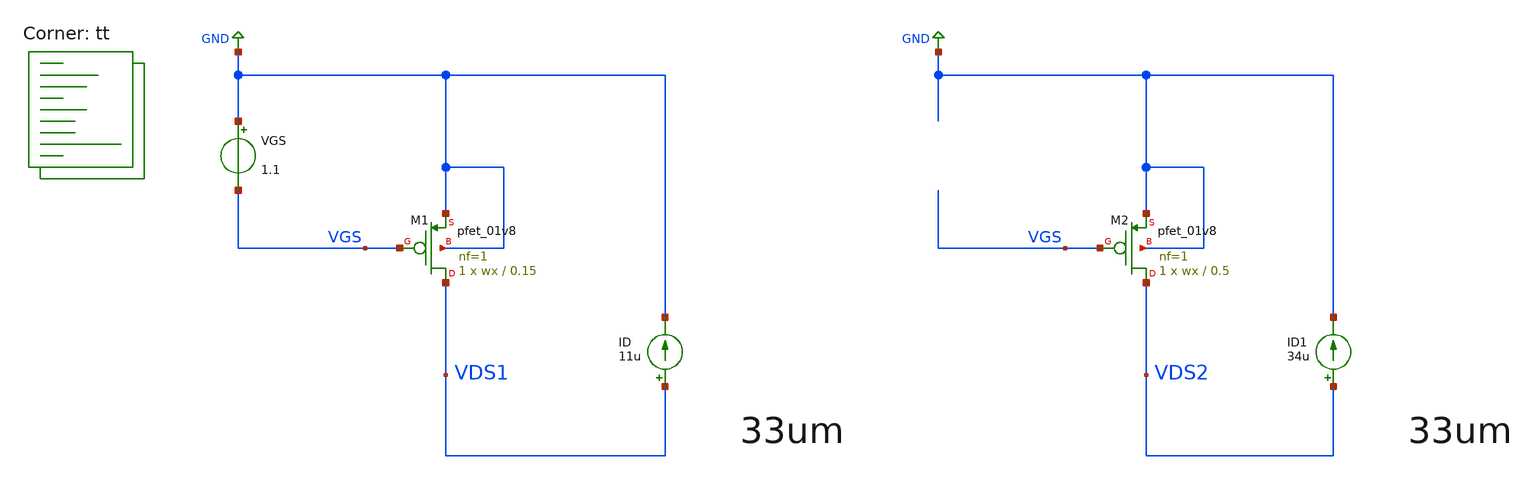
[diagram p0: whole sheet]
** sch_path: projects/opamp/xschem_ngspice/vgs_id_sweep_pfet_2.sch
**.subckt vgs_id_sweep_pfet_2
VGS GND VGS 1.1
ID VDS1 GND 11u
XM1 VDS1 VGS GND GND sky130_fd_pr__pfet_01v8 L=0.15 W=wx nf=1 ad='int((nf+1)/2) * W/nf * 0.29' as='int((nf+2)/2) * W/nf * 0.29'
+ pd='2*int((nf+1)/2) * (W/nf + 0.29)' ps='2*int((nf+2)/2) * (W/nf + 0.29)' nrd='0.29 / W' nrs='0.29 / W'
+ sa=0 sb=0 sd=0 mult=1 m=1
ID1 VDS2 GND 34u
XM2 VDS2 VGS GND GND sky130_fd_pr__pfet_01v8 L=0.5 W=wx nf=1 ad='int((nf+1)/2) * W/nf * 0.29' as='int((nf+2)/2) * W/nf * 0.29'
+ pd='2*int((nf+1)/2) * (W/nf + 0.29)' ps='2*int((nf+2)/2) * (W/nf + 0.29)' nrd='0.29 / W' nrs='0.29 / W'
+ sa=0 sb=0 sd=0 mult=1 m=1
**** begin user architecture code
.lib $::SKYWATER_MODELS/sky130.lib.spice tt




.option method=gear
.option wnflag=1
.option savecurrents

.save @m.xm1.msky130_fd_pr__pfet_01v8[gm] @m.xm1.msky130_fd_pr__pfet_01v8[W] @m.xm1.msky130_fd_pr__pfet_01v8[vth] @m.xm1.msky130_fd_pr__pfet_01v8[gds] @m.xm2.msky130_fd_pr__pfet_01v8[gm] @m.xm2.msky130_fd_pr__pfet_01v8[W] @m.xm2.msky130_fd_pr__pfet_01v8[vth] @m.xm2.msky130_fd_pr__pfet_01v8[gds] @m.xm3.msky130_fd_pr__pfet_01v8[gm] @m.xm3.msky130_fd_pr__pfet_01v8[W] @m.xm3.msky130_fd_pr__pfet_01v8[vth] @m.xm3.msky130_fd_pr__pfet_01v8[gds] @m.xm4.msky130_fd_pr__pfet_01v8[gm] @m.xm4.msky130_fd_pr__pfet_01v8[W] @m.xm4.msky130_fd_pr__pfet_01v8[vth] @m.xm4.msky130_fd_pr__pfet_01v8[gds] @m.xm5.msky130_fd_pr__pfet_01v8[gm] @m.xm5.msky130_fd_pr__pfet_01v8[W] @m.xm5.msky130_fd_pr__pfet_01v8[vth] @m.xm5.msky130_fd_pr__pfet_01v8[gds] @m.xm6.msky130_fd_pr__pfet_01v8[gm] @m.xm6.msky130_fd_pr__pfet_01v8[W] @m.xm6.msky130_fd_pr__pfet_01v8[vth] @m.xm6.msky130_fd_pr__pfet_01v8[gds] @m.xm7.msky130_fd_pr__pfet_01v8[gm] @m.xm7.msky130_fd_pr__pfet_01v8[W] @m.xm7.msky130_fd_pr__pfet_01v8[vth] @m.xm7.msky130_fd_pr__pfet_01v8[gds] @m.xm8.msky130_fd_pr__pfet_01v8[gm] @m.xm8.msky130_fd_pr__pfet_01v8[W] @m.xm8.msky130_fd_pr__pfet_01v8[vth] @m.xm8.msky130_fd_pr__pfet_01v8[gds]

.param wx=1
.dc VGS 0 1.8 0.001

.control

  let start_w = 1
  let stop_w = 100
  let delta_w = 1
  let w_act = start_w
  while w_act le stop_w
    alterparam wx = $&w_act
    reset
    save all
    run
    remzerovec
    write vgs_id_sweep_pfet_2.raw
    let w_act = w_act + delta_w
    set appendwrite
  end

* let rout = deriv(vds6)/deriv(@m.xm6.msky130_fd_pr__pfet_01v8[id])
* plot rout

show

.endc




**** end user architecture code
**.ends
.GLOBAL GND
.end
